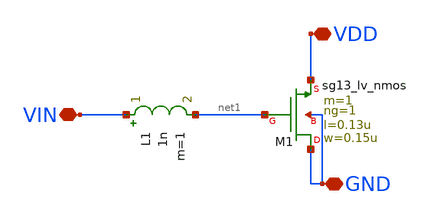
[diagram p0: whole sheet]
** sch_path: LVS/LAYOUT/test_inductance/test_inductance.sch
**.subckt test_inductance VDD VIN GND
*.iopin VDD
*.iopin VIN
*.iopin GND
XM1 GND net1 VDD GND sg13_lv_nmos w=0.15u l=0.13u ng=1 m=1 mm_ok=1
L1 VIN net1 1n m=1
**.ends
.end
